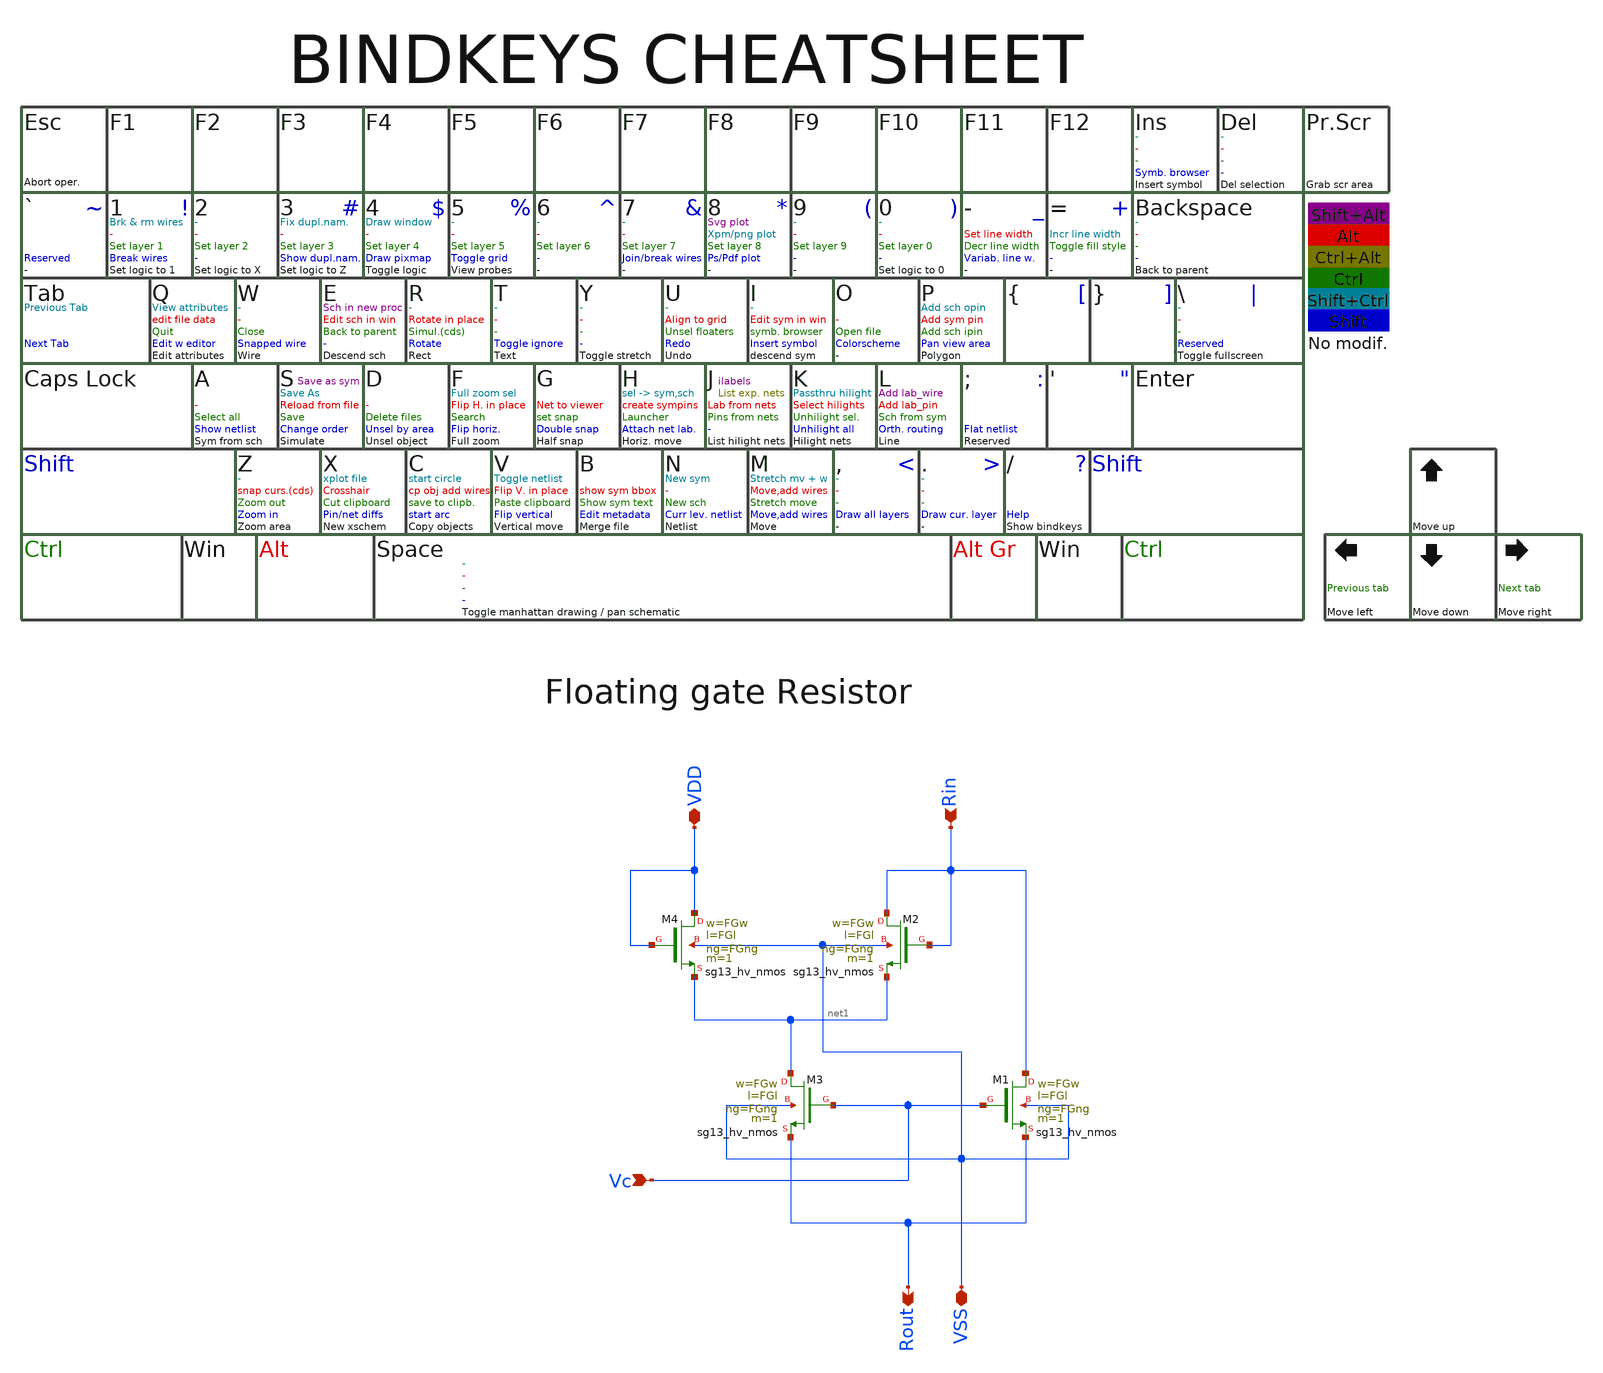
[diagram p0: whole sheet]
** sch_path: macros/heichips26_analog_project/macros/floating-gate/schematic/xschem/floating-gate.sch
**.subckt floating-gate VDD Rin Rout Vc VSS
*.iopin VDD
*.ipin Rin
*.opin Rout
*.ipin Vc
*.iopin VSS
XM2 Rin Rin net1 VSS sg13_hv_nmos w=FGw l=FGl ng=FGng m=1 mm_ok=1
XM4 VDD VDD net1 VSS sg13_hv_nmos w=FGw l=FGl ng=FGng m=1 mm_ok=1
XM3 net1 Vc Rout VSS sg13_hv_nmos w=FGw l=FGl ng=FGng m=1 mm_ok=1
XM1 Rin Vc Rout VSS sg13_hv_nmos w=FGw l=FGl ng=FGng m=1 mm_ok=1
**** begin user architecture code
FGw=2u
FGl=4u
FGng=1
**** end user architecture code
**.ends
.end
